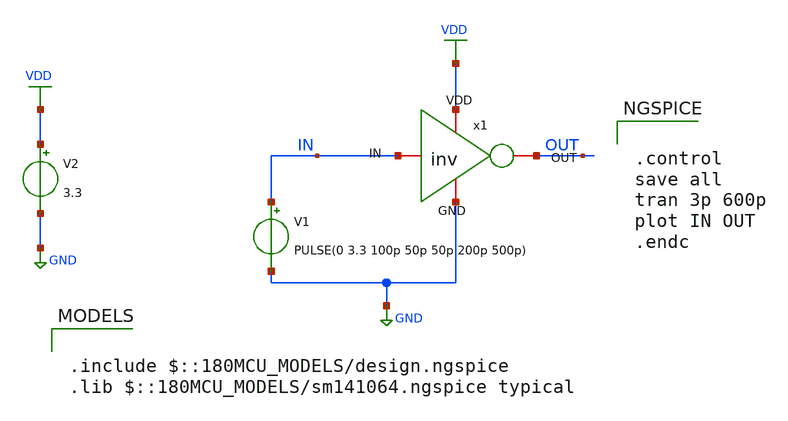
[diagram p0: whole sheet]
** sch_path: analog/design/inv/inv_tb.sch
**.subckt inv_tb
V1 IN GND PULSE(0 3.3 100p 50p 50p 200p 500p)
V2 VDD GND 3.3
x1 VDD IN OUT GND inv
**** begin user architecture code


.control
save all
tran 3p 600p
plot IN OUT
.endc



.include $::180MCU_MODELS/design.ngspice
.lib $::180MCU_MODELS/sm141064.ngspice typical

**** end user architecture code
**.ends

* expanding   symbol:  /home/econde/projects/C01/design/test/inv.sym # of pins=4
** sym_path: analog/design/inv/inv.sym
** sch_path: analog/design/inv/inv.sch
.subckt inv VDD IN OUT GND
*.iopin OUT
*.iopin VDD
*.iopin GND
*.iopin IN
XM1 OUT IN VDD VDD pfet_03v3 L=0.28u W=0.44u nf=1 ad='int((nf+1)/2) * W/nf * 0.18u' as='int((nf+2)/2) * W/nf * 0.18u'
+ pd='2*int((nf+1)/2) * (W/nf + 0.18u)' ps='2*int((nf+2)/2) * (W/nf + 0.18u)' nrd='0.18u / W' nrs='0.18u / W'
+ sa=0 sb=0 sd=0 m=1
XM2 OUT IN GND GND nfet_03v3 L=0.28u W=0.22u nf=1 ad='int((nf+1)/2) * W/nf * 0.18u' as='int((nf+2)/2) * W/nf * 0.18u'
+ pd='2*int((nf+1)/2) * (W/nf + 0.18u)' ps='2*int((nf+2)/2) * (W/nf + 0.18u)' nrd='0.18u / W' nrs='0.18u / W'
+ sa=0 sb=0 sd=0 m=1
.ends

.GLOBAL VDD
.GLOBAL GND
.end
